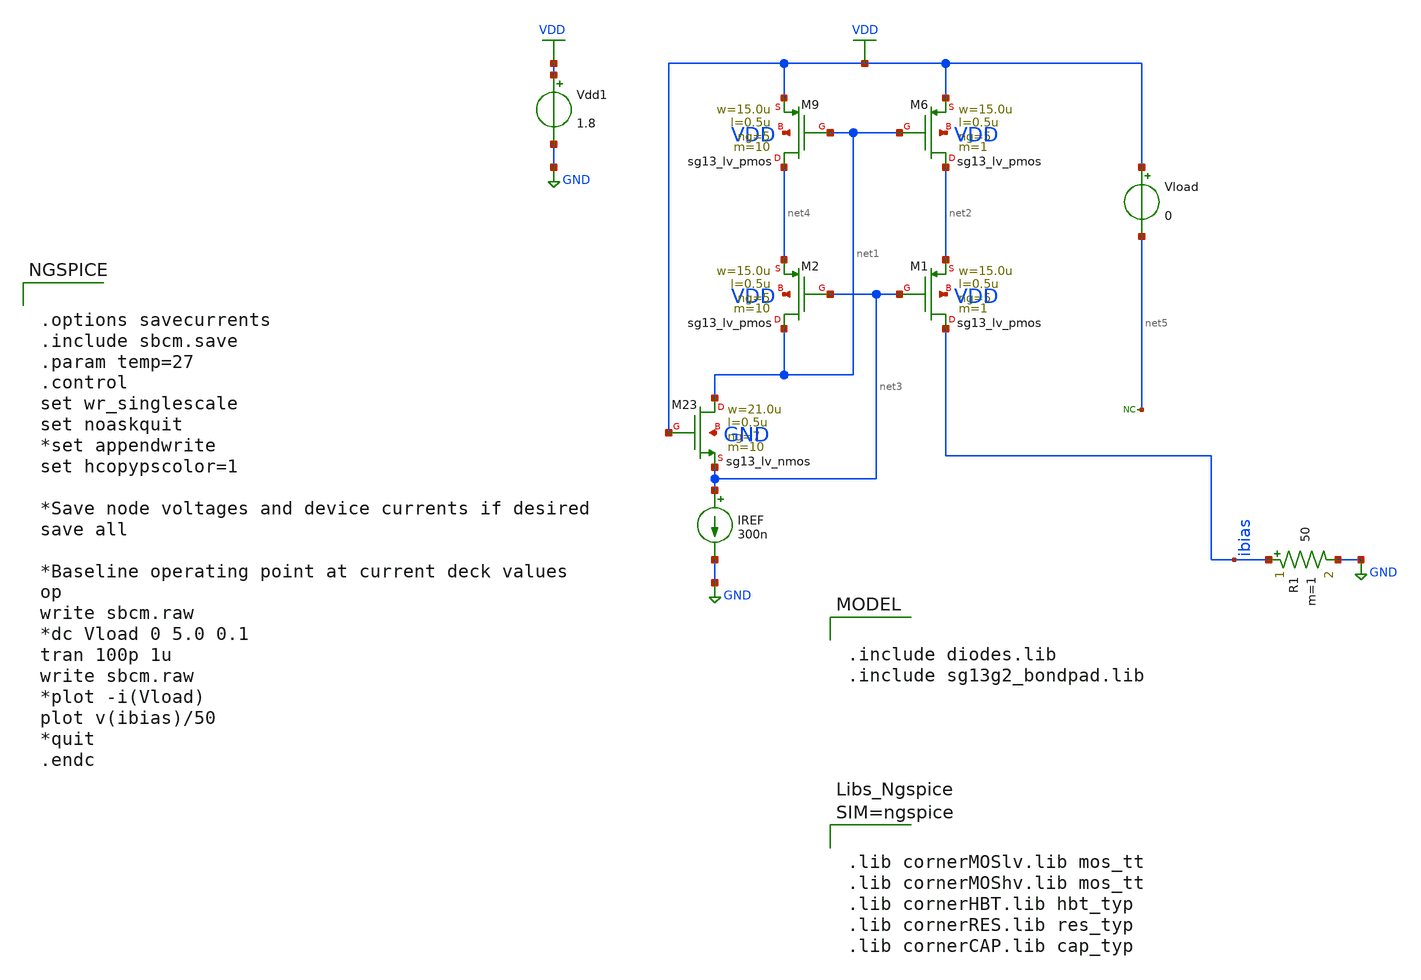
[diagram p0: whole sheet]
** sch_path: blocks/composite/dpi_adexp_neuron/design_data/xschem/dev/sbcm.sch
**.subckt sbcm
Vdd1 VDD GND 1.8
XM6 net2 net1 VDD VDD sg13_lv_pmos w=15.0u l=0.5u ng=5 m=1 mm_ok=1
XM9 net4 net1 VDD VDD sg13_lv_pmos w=15.0u l=0.5u ng=5 m=10 mm_ok=1
XM1 ibias net3 net2 VDD sg13_lv_pmos w=15.0u l=0.5u ng=5 m=1 mm_ok=1
XM2 net1 net3 net4 VDD sg13_lv_pmos w=15.0u l=0.5u ng=5 m=10 mm_ok=1
IREF net3 GND 300n
R1 ibias GND 50 m=1
XM23 net1 VDD net3 GND sg13_lv_nmos w=21.0u l=0.5u ng=7 m=10 mm_ok=1
Vload VDD net5 0
* noconn #net5
**** begin user architecture code

.include diodes.lib
.include sg13g2_bondpad.lib



.options savecurrents
.include sbcm.save
.param temp=27
.control
set wr_singlescale
set noaskquit
*set appendwrite
set hcopypscolor=1

*Save node voltages and device currents if desired
save all

*Baseline operating point at current deck values
op
write sbcm.raw
*dc Vload 0 5.0 0.1
tran 100p 1u
write sbcm.raw
*plot -i(Vload)
plot v(ibias)/50
*quit
.endc





.lib cornerMOSlv.lib mos_tt
.lib cornerMOShv.lib mos_tt
.lib cornerHBT.lib hbt_typ
.lib cornerRES.lib res_typ
.lib cornerCAP.lib cap_typ



**** end user architecture code
**.ends
.GLOBAL GND
.GLOBAL VDD
.end
